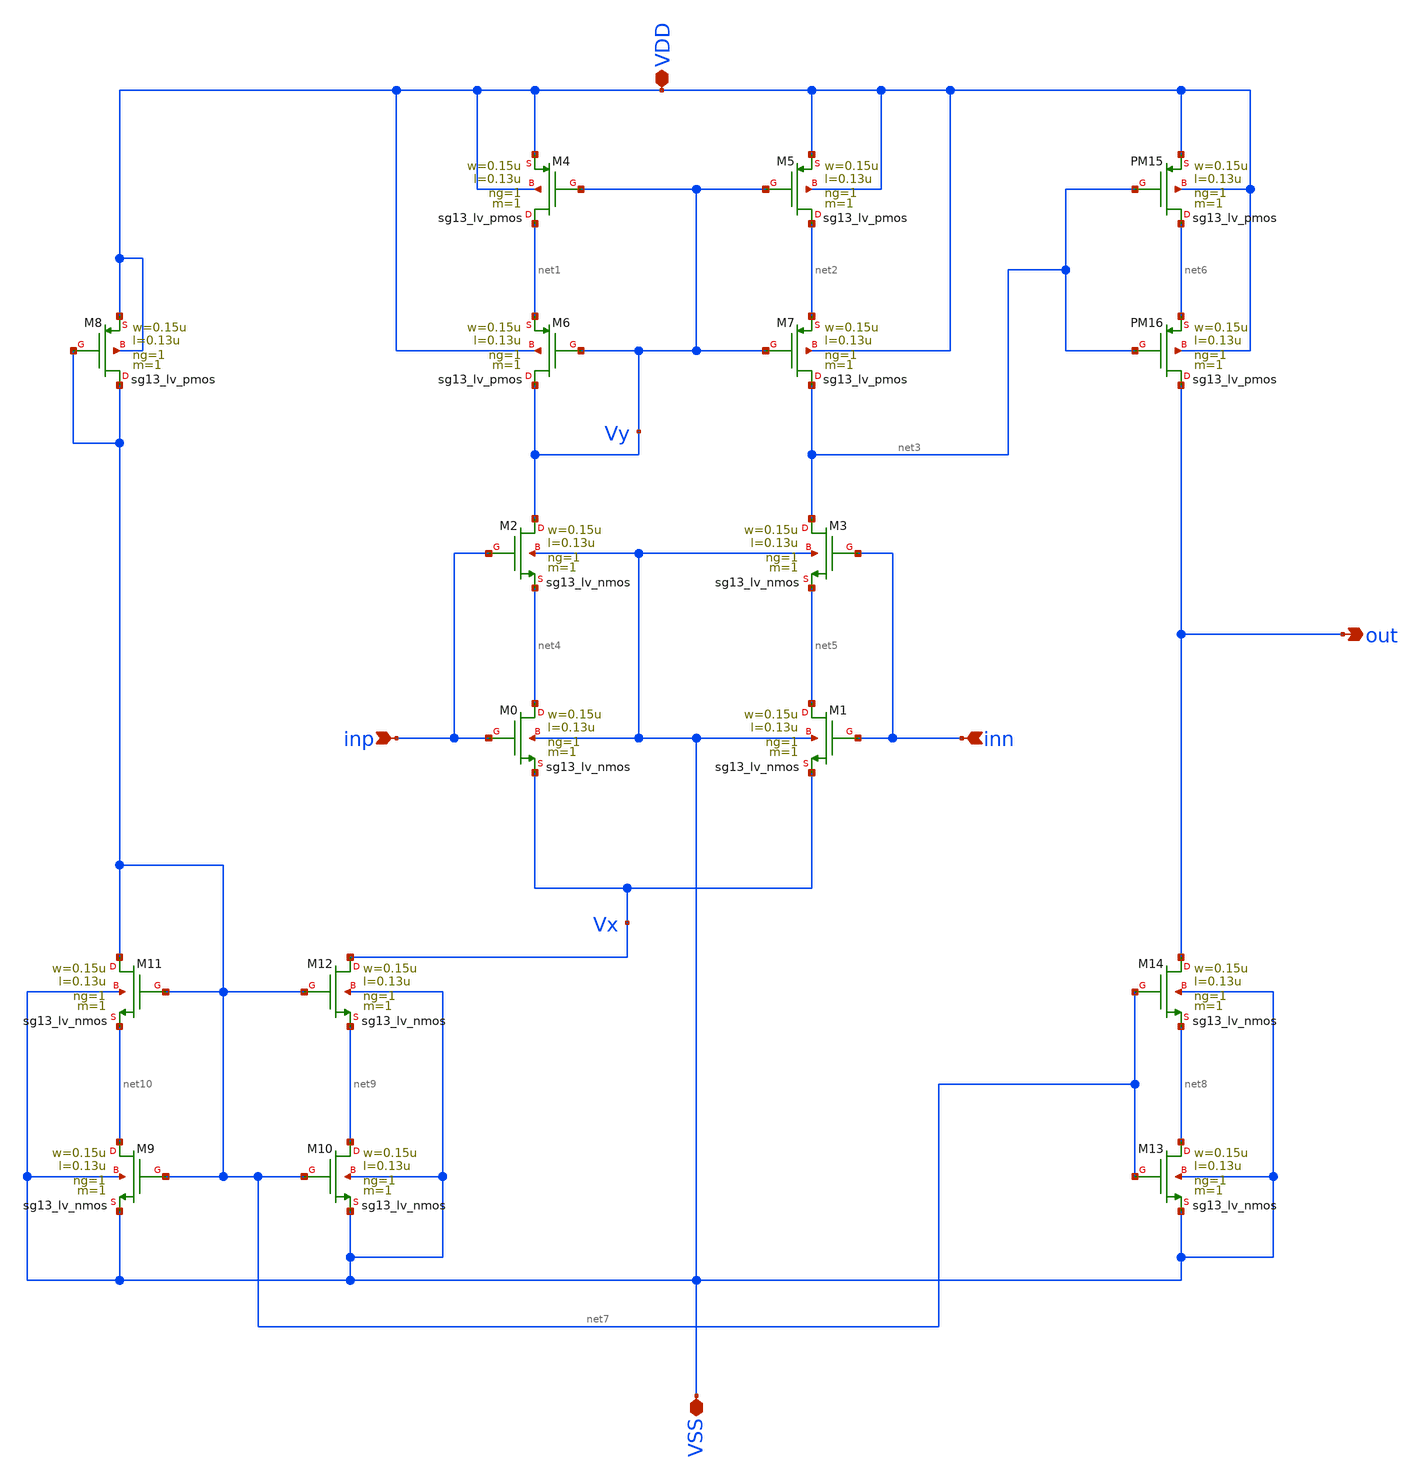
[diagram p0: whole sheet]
** sch_path: xschem/Two_state_self_cascode_OTA.sch
**.subckt Two_state_self_cascode_OTA inp inn out VDD VSS
*.ipin inp
*.ipin inn
*.opin out
*.iopin VDD
*.iopin VSS
XM5 net2 Vy VDD VDD sg13_lv_pmos w=0.15u l=0.13u ng=1 m=1 mm_ok=1
XM7 net3 Vy net2 VDD sg13_lv_pmos w=0.15u l=0.13u ng=1 m=1 mm_ok=1
XM4 net1 Vy VDD VDD sg13_lv_pmos w=0.15u l=0.13u ng=1 m=1 mm_ok=1
XM6 Vy Vy net1 VDD sg13_lv_pmos w=0.15u l=0.13u ng=1 m=1 mm_ok=1
XM2 Vy inp net4 VSS sg13_lv_nmos w=0.15u l=0.13u ng=1 m=1 mm_ok=1
XM0 net4 inp Vx VSS sg13_lv_nmos w=0.15u l=0.13u ng=1 m=1 mm_ok=1
XM3 net3 inn net5 VSS sg13_lv_nmos w=0.15u l=0.13u ng=1 m=1 mm_ok=1
XM1 net5 inn Vx VSS sg13_lv_nmos w=0.15u l=0.13u ng=1 m=1 mm_ok=1
XPM15 net6 net3 VDD VDD sg13_lv_pmos w=0.15u l=0.13u ng=1 m=1 mm_ok=1
XPM16 out net3 net6 VDD sg13_lv_pmos w=0.15u l=0.13u ng=1 m=1 mm_ok=1
XM14 out net7 net8 VSS sg13_lv_nmos w=0.15u l=0.13u ng=1 m=1 mm_ok=1
XM13 net8 net7 VSS VSS sg13_lv_nmos w=0.15u l=0.13u ng=1 m=1 mm_ok=1
XM12 Vx net7 net9 VSS sg13_lv_nmos w=0.15u l=0.13u ng=1 m=1 mm_ok=1
XM10 net9 net7 VSS VSS sg13_lv_nmos w=0.15u l=0.13u ng=1 m=1 mm_ok=1
XM11 net7 net7 net10 VSS sg13_lv_nmos w=0.15u l=0.13u ng=1 m=1 mm_ok=1
XM9 net10 net7 VSS VSS sg13_lv_nmos w=0.15u l=0.13u ng=1 m=1 mm_ok=1
XM8 net7 net7 VDD VDD sg13_lv_pmos w=0.15u l=0.13u ng=1 m=1 mm_ok=1
**.ends
.end
